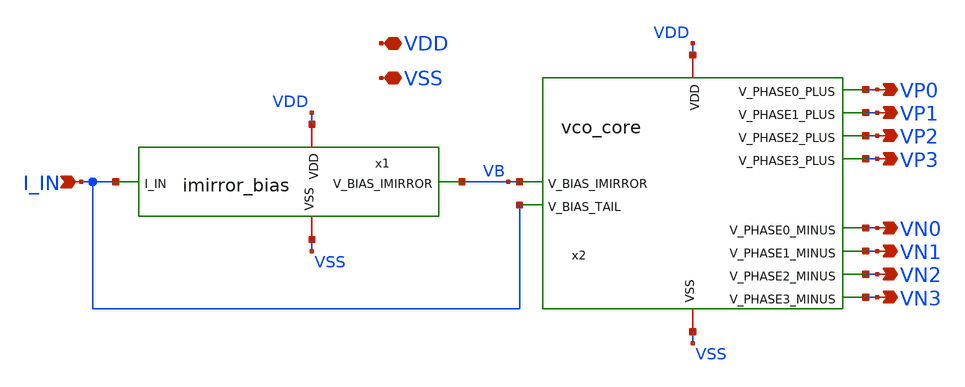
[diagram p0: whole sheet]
** sch_path: xschem/vco.sch
**.subckt vco I_IN VP0 VP1 VP2 VP3 VN0 VN1 VN2 VN3 VDD VSS
*.ipin I_IN
*.opin VP0
*.opin VP1
*.opin VP2
*.opin VP3
*.opin VN0
*.opin VN1
*.opin VN2
*.opin VN3
*.iopin VDD
*.iopin VSS
x1 VDD VB I_IN VSS imirror_bias
x2 VB VDD I_IN VSS VP2 VP1 VP3 VP0 VN2 VN1 VN3 VN0 vco_core
**.ends
.end
